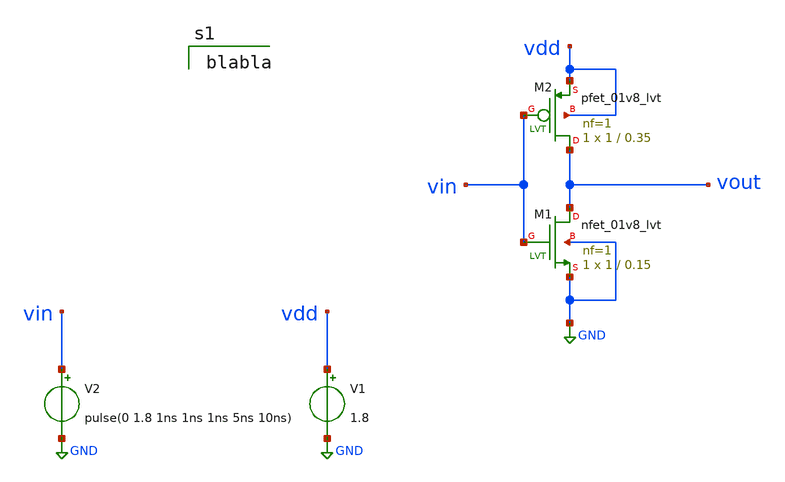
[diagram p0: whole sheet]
** sch_path: MOSFET_analysis/mosfet_analysis.sch
**.subckt mosfet_analysis
V1 vdd GND 1.8
V2 vin GND pulse(0 1.8 1ns 1ns 1ns 5ns 10ns)
XM1 vout vin GND GND sky130_fd_pr__nfet_01v8_lvt L=0.15 W=1 nf=1 ad='int((nf+1)/2) * W/nf * 0.29' as='int((nf+2)/2) * W/nf * 0.29'
+ pd='2*int((nf+1)/2) * (W/nf + 0.29)' ps='2*int((nf+2)/2) * (W/nf + 0.29)' nrd='0.29 / W' nrs='0.29 / W'
+ sa=0 sb=0 sd=0 mult=1 m=1
XM2 vout vin vdd vdd sky130_fd_pr__pfet_01v8_lvt L=0.35 W=1 nf=1 ad='int((nf+1)/2) * W/nf * 0.29' as='int((nf+2)/2) * W/nf * 0.29'
+ pd='2*int((nf+1)/2) * (W/nf + 0.29)' ps='2*int((nf+2)/2) * (W/nf + 0.29)' nrd='0.29 / W' nrs='0.29 / W'
+ sa=0 sb=0 sd=0 mult=1 m=1
**** begin user architecture code

blabla

**** end user architecture code
**.ends
.GLOBAL GND
.end
